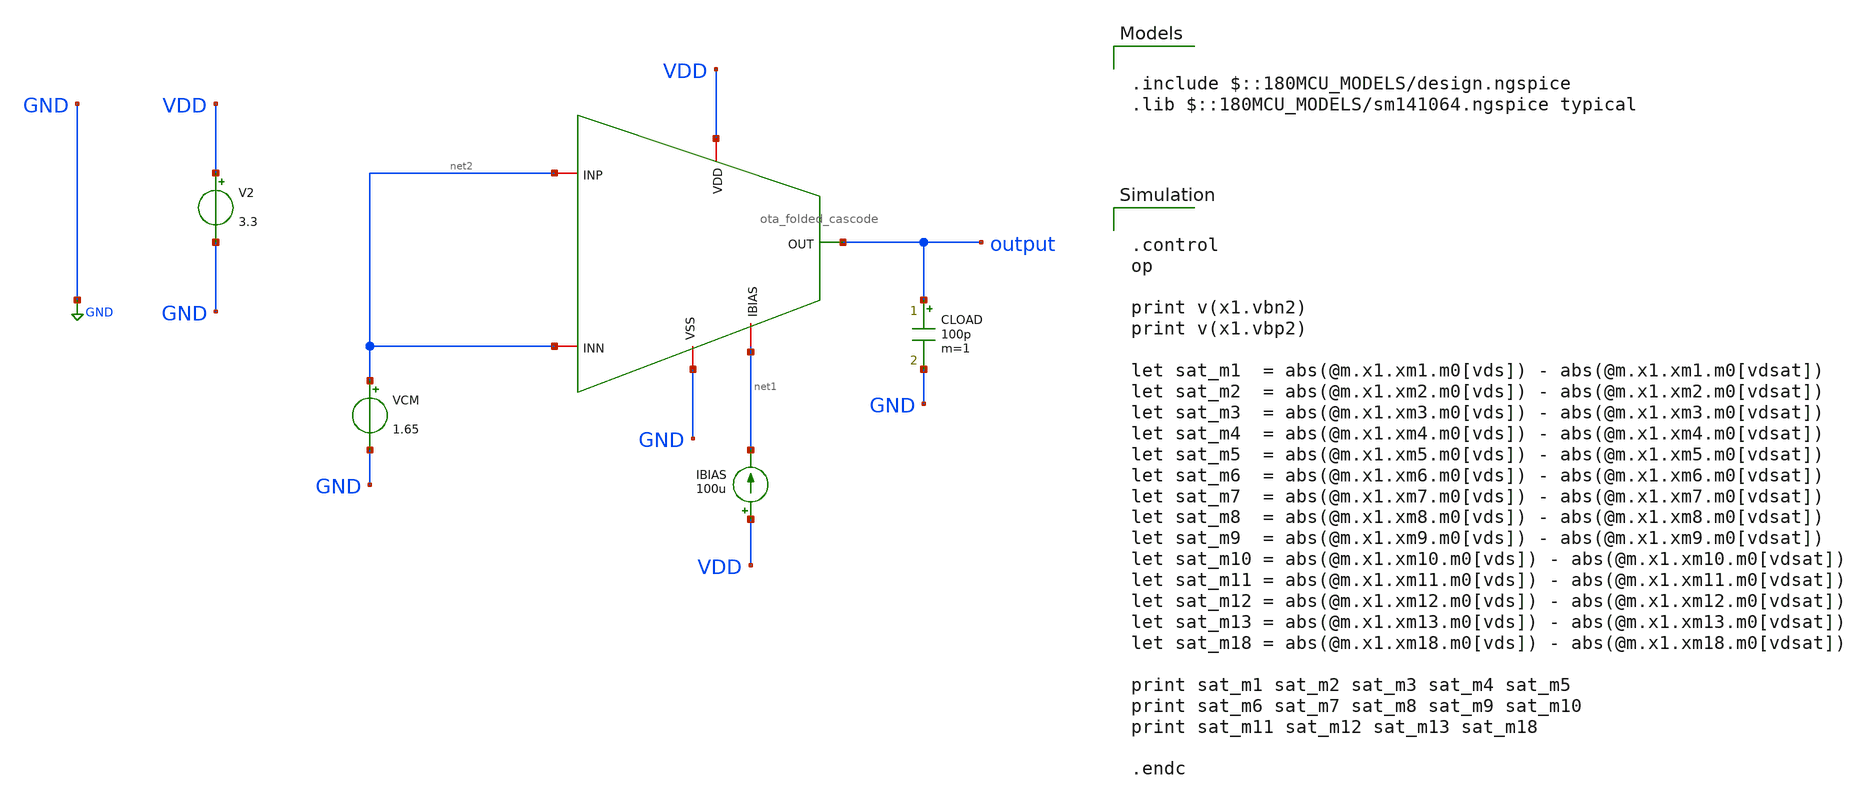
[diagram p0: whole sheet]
** sch_path: designs/libs/core_amps/ota_folded_cascode/op_vdsat_tb.sch
**.subckt op_vdsat_tb
IBIAS VDD net1 100u
V2 VDD GND 3.3
CLOAD output GND 100p m=1
VCM net2 GND 1.65
x1 VDD GND output net2 net2 net1 ota_folded_cascode
**** begin user architecture code

.include $::180MCU_MODELS/design.ngspice
.lib $::180MCU_MODELS/sm141064.ngspice typical



.control
op

print v(x1.vbn2)
print v(x1.vbp2)

let sat_m1  = abs(@m.x1.xm1.m0[vds]) - abs(@m.x1.xm1.m0[vdsat])
let sat_m2  = abs(@m.x1.xm2.m0[vds]) - abs(@m.x1.xm2.m0[vdsat])
let sat_m3  = abs(@m.x1.xm3.m0[vds]) - abs(@m.x1.xm3.m0[vdsat])
let sat_m4  = abs(@m.x1.xm4.m0[vds]) - abs(@m.x1.xm4.m0[vdsat])
let sat_m5  = abs(@m.x1.xm5.m0[vds]) - abs(@m.x1.xm5.m0[vdsat])
let sat_m6  = abs(@m.x1.xm6.m0[vds]) - abs(@m.x1.xm6.m0[vdsat])
let sat_m7  = abs(@m.x1.xm7.m0[vds]) - abs(@m.x1.xm7.m0[vdsat])
let sat_m8  = abs(@m.x1.xm8.m0[vds]) - abs(@m.x1.xm8.m0[vdsat])
let sat_m9  = abs(@m.x1.xm9.m0[vds]) - abs(@m.x1.xm9.m0[vdsat])
let sat_m10 = abs(@m.x1.xm10.m0[vds]) - abs(@m.x1.xm10.m0[vdsat])
let sat_m11 = abs(@m.x1.xm11.m0[vds]) - abs(@m.x1.xm11.m0[vdsat])
let sat_m12 = abs(@m.x1.xm12.m0[vds]) - abs(@m.x1.xm12.m0[vdsat])
let sat_m13 = abs(@m.x1.xm13.m0[vds]) - abs(@m.x1.xm13.m0[vdsat])
let sat_m18 = abs(@m.x1.xm18.m0[vds]) - abs(@m.x1.xm18.m0[vdsat])

print sat_m1 sat_m2 sat_m3 sat_m4 sat_m5
print sat_m6 sat_m7 sat_m8 sat_m9 sat_m10
print sat_m11 sat_m12 sat_m13 sat_m18

.endc



**** end user architecture code
**.ends
.GLOBAL GND
.end
